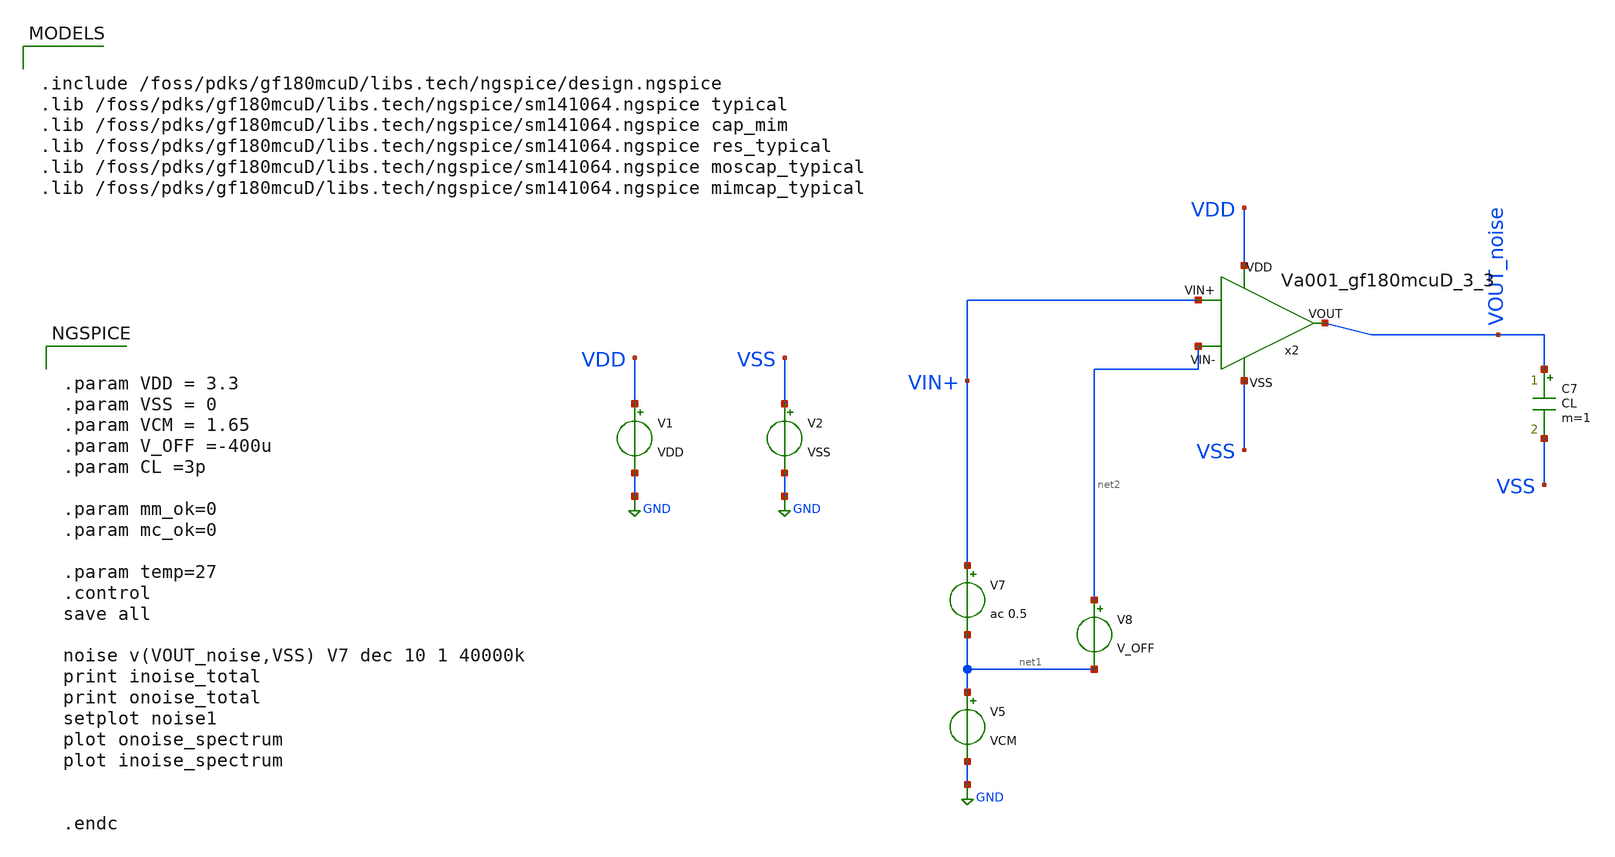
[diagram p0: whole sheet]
** sch_path: Learning/single_ended_amplifiers/VA001_series/Design_and_Analysis_of_Two-Stage_CMOS_Operational_Amplifier_for_Fluorescence_Signal_Processing_gf180mcu_3_3V/amplifier_design/noise.sch
**.subckt noise
V5 net1 GND VCM
V7 VIN+ net1 ac 0.5
V8 net2 net1 V_OFF
V1 VDD GND VDD
V2 VSS GND VSS
C7 VOUT_noise VSS CL m=1
x2 VDD VSS net2 VIN+ VOUT_noise Va001_gf180mcuD_3_3
**** begin user architecture code

.include /foss/pdks/gf180mcuD/libs.tech/ngspice/design.ngspice
.lib /foss/pdks/gf180mcuD/libs.tech/ngspice/sm141064.ngspice typical
.lib /foss/pdks/gf180mcuD/libs.tech/ngspice/sm141064.ngspice cap_mim
.lib /foss/pdks/gf180mcuD/libs.tech/ngspice/sm141064.ngspice res_typical
.lib /foss/pdks/gf180mcuD/libs.tech/ngspice/sm141064.ngspice moscap_typical
.lib /foss/pdks/gf180mcuD/libs.tech/ngspice/sm141064.ngspice mimcap_typical

**** end user architecture code
**.ends
.GLOBAL GND
**** begin user architecture code


.param VDD = 3.3
.param VSS = 0
.param VCM = 1.65
.param V_OFF =-400u
.param CL =3p

.param mm_ok=0
.param mc_ok=0

.param temp=27
.control
save all

noise v(VOUT_noise,VSS) V7 dec 10 1 40000k
print inoise_total
print onoise_total
setplot noise1
plot onoise_spectrum
plot inoise_spectrum


.endc


**** end user architecture code
.end
